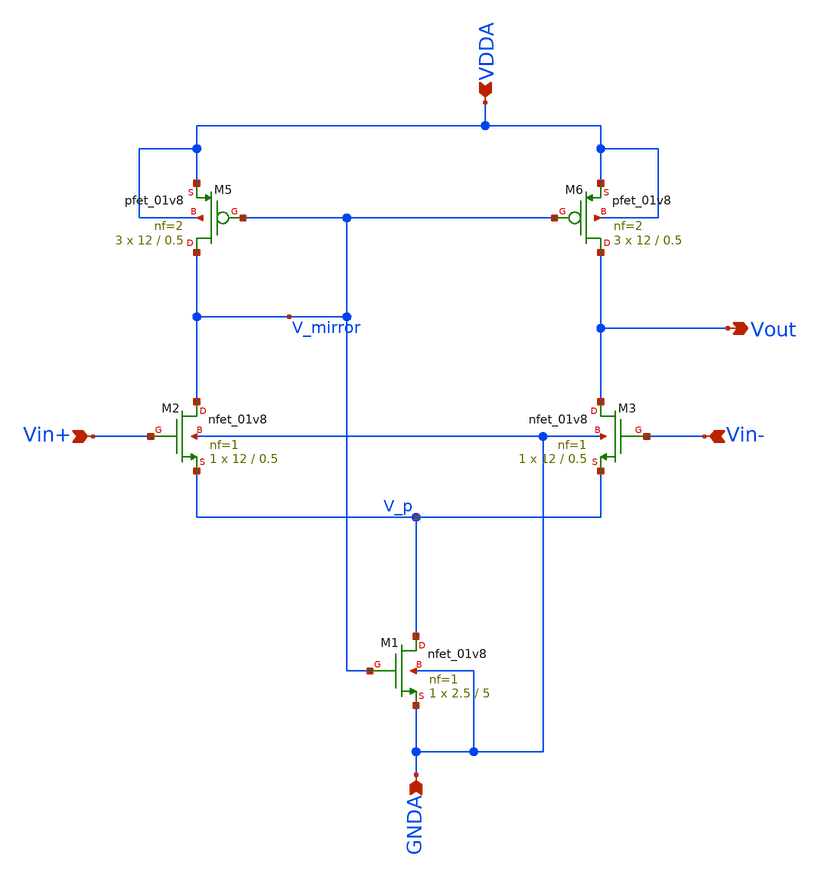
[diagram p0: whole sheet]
** sch_path: projects/ASU/EEE572/schematic/opamp_bandgap_5.sch
**.subckt opamp_bandgap_5 Vin+ Vout Vin- GNDA VDDA
*.ipin Vin+
*.opin Vout
*.ipin Vin-
*.ipin GNDA
*.ipin VDDA
XM1 V_p V_mirror GNDA GNDA sky130_fd_pr__nfet_01v8 L=5 W=2.5 nf=1 ad='int((nf+1)/2) * W/nf * 0.29' as='int((nf+2)/2) * W/nf * 0.29'
+ pd='2*int((nf+1)/2) * (W/nf + 0.29)' ps='2*int((nf+2)/2) * (W/nf + 0.29)' nrd='0.29 / W' nrs='0.29 / W'
+ sa=0 sb=0 sd=0 mult=1 m=1
XM2 V_mirror Vin+ V_p GNDA sky130_fd_pr__nfet_01v8 L=0.5 W=12 nf=1 ad='int((nf+1)/2) * W/nf * 0.29' as='int((nf+2)/2) * W/nf * 0.29'
+ pd='2*int((nf+1)/2) * (W/nf + 0.29)' ps='2*int((nf+2)/2) * (W/nf + 0.29)' nrd='0.29 / W' nrs='0.29 / W'
+ sa=0 sb=0 sd=0 mult=1 m=1
XM3 Vout Vin- V_p GNDA sky130_fd_pr__nfet_01v8 L=0.5 W=12 nf=1 ad='int((nf+1)/2) * W/nf * 0.29' as='int((nf+2)/2) * W/nf * 0.29'
+ pd='2*int((nf+1)/2) * (W/nf + 0.29)' ps='2*int((nf+2)/2) * (W/nf + 0.29)' nrd='0.29 / W' nrs='0.29 / W'
+ sa=0 sb=0 sd=0 mult=1 m=1
XM5 V_mirror V_mirror VDDA VDDA sky130_fd_pr__pfet_01v8 L=0.5 W=12 nf=2 ad='int((nf+1)/2) * W/nf * 0.29'
+ as='int((nf+2)/2) * W/nf * 0.29' pd='2*int((nf+1)/2) * (W/nf + 0.29)' ps='2*int((nf+2)/2) * (W/nf + 0.29)'
+ nrd='0.29 / W' nrs='0.29 / W' sa=0 sb=0 sd=0 mult=3 m=3
XM6 Vout V_mirror VDDA VDDA sky130_fd_pr__pfet_01v8 L=0.5 W=12 nf=2 ad='int((nf+1)/2) * W/nf * 0.29'
+ as='int((nf+2)/2) * W/nf * 0.29' pd='2*int((nf+1)/2) * (W/nf + 0.29)' ps='2*int((nf+2)/2) * (W/nf + 0.29)'
+ nrd='0.29 / W' nrs='0.29 / W' sa=0 sb=0 sd=0 mult=3 m=3
**.ends
.end
